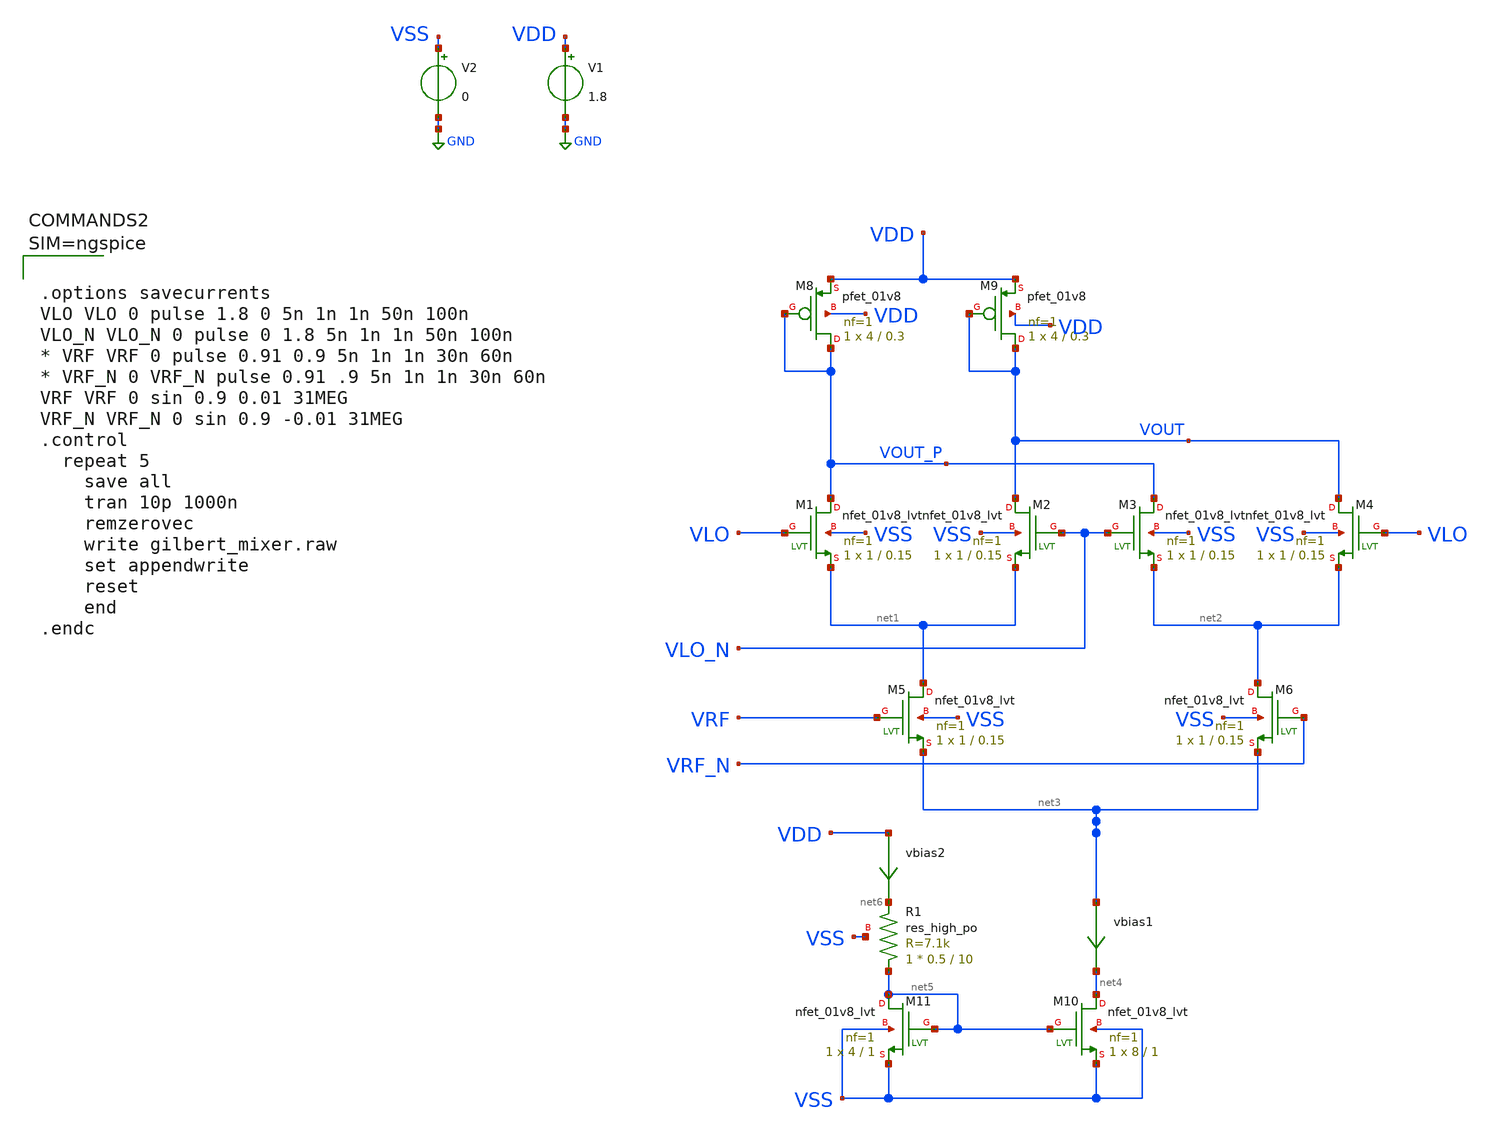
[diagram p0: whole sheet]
** sch_path: xschem/gilbert_mixer.sch
**.subckt gilbert_mixer
XM1 VOUT_P VLO net1 VSS sky130_fd_pr__nfet_01v8_lvt L=0.15 W=1 nf=1 ad='int((nf+1)/2) * W/nf * 0.29'
+ as='int((nf+2)/2) * W/nf * 0.29' pd='2*int((nf+1)/2) * (W/nf + 0.29)' ps='2*int((nf+2)/2) * (W/nf + 0.29)'
+ nrd='0.29 / W' nrs='0.29 / W' sa=0 sb=0 sd=0 mult=1 m=1
XM2 VOUT VLO_N net1 VSS sky130_fd_pr__nfet_01v8_lvt L=0.15 W=1 nf=1 ad='int((nf+1)/2) * W/nf * 0.29'
+ as='int((nf+2)/2) * W/nf * 0.29' pd='2*int((nf+1)/2) * (W/nf + 0.29)' ps='2*int((nf+2)/2) * (W/nf + 0.29)'
+ nrd='0.29 / W' nrs='0.29 / W' sa=0 sb=0 sd=0 mult=1 m=1
XM3 VOUT_P VLO_N net2 VSS sky130_fd_pr__nfet_01v8_lvt L=0.15 W=1 nf=1 ad='int((nf+1)/2) * W/nf * 0.29'
+ as='int((nf+2)/2) * W/nf * 0.29' pd='2*int((nf+1)/2) * (W/nf + 0.29)' ps='2*int((nf+2)/2) * (W/nf + 0.29)'
+ nrd='0.29 / W' nrs='0.29 / W' sa=0 sb=0 sd=0 mult=1 m=1
XM4 VOUT VLO net2 VSS sky130_fd_pr__nfet_01v8_lvt L=0.15 W=1 nf=1 ad='int((nf+1)/2) * W/nf * 0.29' as='int((nf+2)/2) * W/nf * 0.29'
+ pd='2*int((nf+1)/2) * (W/nf + 0.29)' ps='2*int((nf+2)/2) * (W/nf + 0.29)' nrd='0.29 / W' nrs='0.29 / W'
+ sa=0 sb=0 sd=0 mult=1 m=1
XM5 net1 VRF net3 VSS sky130_fd_pr__nfet_01v8_lvt L=0.15 W=1 nf=1 ad='int((nf+1)/2) * W/nf * 0.29' as='int((nf+2)/2) * W/nf * 0.29'
+ pd='2*int((nf+1)/2) * (W/nf + 0.29)' ps='2*int((nf+2)/2) * (W/nf + 0.29)' nrd='0.29 / W' nrs='0.29 / W'
+ sa=0 sb=0 sd=0 mult=1 m=1
XM6 net2 VRF_N net3 VSS sky130_fd_pr__nfet_01v8_lvt L=0.15 W=1 nf=1 ad='int((nf+1)/2) * W/nf * 0.29'
+ as='int((nf+2)/2) * W/nf * 0.29' pd='2*int((nf+1)/2) * (W/nf + 0.29)' ps='2*int((nf+2)/2) * (W/nf + 0.29)'
+ nrd='0.29 / W' nrs='0.29 / W' sa=0 sb=0 sd=0 mult=1 m=1
XM8 VOUT_P VOUT_P VDD VDD sky130_fd_pr__pfet_01v8 L=0.3 W=4 nf=1 ad='int((nf+1)/2) * W/nf * 0.29' as='int((nf+2)/2) * W/nf * 0.29'
+ pd='2*int((nf+1)/2) * (W/nf + 0.29)' ps='2*int((nf+2)/2) * (W/nf + 0.29)' nrd='0.29 / W' nrs='0.29 / W'
+ sa=0 sb=0 sd=0 mult=1 m=1
XM9 VOUT VOUT VDD VDD sky130_fd_pr__pfet_01v8 L=0.3 W=4 nf=1 ad='int((nf+1)/2) * W/nf * 0.29' as='int((nf+2)/2) * W/nf * 0.29'
+ pd='2*int((nf+1)/2) * (W/nf + 0.29)' ps='2*int((nf+2)/2) * (W/nf + 0.29)' nrd='0.29 / W' nrs='0.29 / W'
+ sa=0 sb=0 sd=0 mult=1 m=1
V1 VDD GND 1.8
V2 VSS GND 0
XM10 net4 net5 VSS VSS sky130_fd_pr__nfet_01v8_lvt L=1 W=8 nf=1 ad='int((nf+1)/2) * W/nf * 0.29' as='int((nf+2)/2) * W/nf * 0.29'
+ pd='2*int((nf+1)/2) * (W/nf + 0.29)' ps='2*int((nf+2)/2) * (W/nf + 0.29)' nrd='0.29 / W' nrs='0.29 / W'
+ sa=0 sb=0 sd=0 mult=1 m=1
vbias1 net3 net4 0
.save i(vbias1)
XR1 net5 net6 VSS sky130_fd_pr__res_high_po W=0.5 L=10 mult=1 m=1
XM11 net5 net5 VSS VSS sky130_fd_pr__nfet_01v8_lvt L=1 W=4 nf=1 ad='int((nf+1)/2) * W/nf * 0.29' as='int((nf+2)/2) * W/nf * 0.29'
+ pd='2*int((nf+1)/2) * (W/nf + 0.29)' ps='2*int((nf+2)/2) * (W/nf + 0.29)' nrd='0.29 / W' nrs='0.29 / W'
+ sa=0 sb=0 sd=0 mult=1 m=1
vbias2 VDD net6 0
.save i(vbias2)
**** begin user architecture code

** opencircuitdesign pdks install
.lib $::SKYWATER_MODELS/sky130.lib.spice tt_mm





.options savecurrents
VLO VLO 0 pulse 1.8 0 5n 1n 1n 50n 100n
VLO_N VLO_N 0 pulse 0 1.8 5n 1n 1n 50n 100n
* VRF VRF 0 pulse 0.91 0.9 5n 1n 1n 30n 60n
* VRF_N 0 VRF_N pulse 0.91 .9 5n 1n 1n 30n 60n
VRF VRF 0 sin 0.9 0.01 31MEG
VRF_N VRF_N 0 sin 0.9 -0.01 31MEG
.control
  repeat 5
    save all
    tran 10p 1000n
    remzerovec
    write gilbert_mixer.raw
    set appendwrite
    reset
    end
.endc



**** end user architecture code
**.ends
.GLOBAL GND
.end
